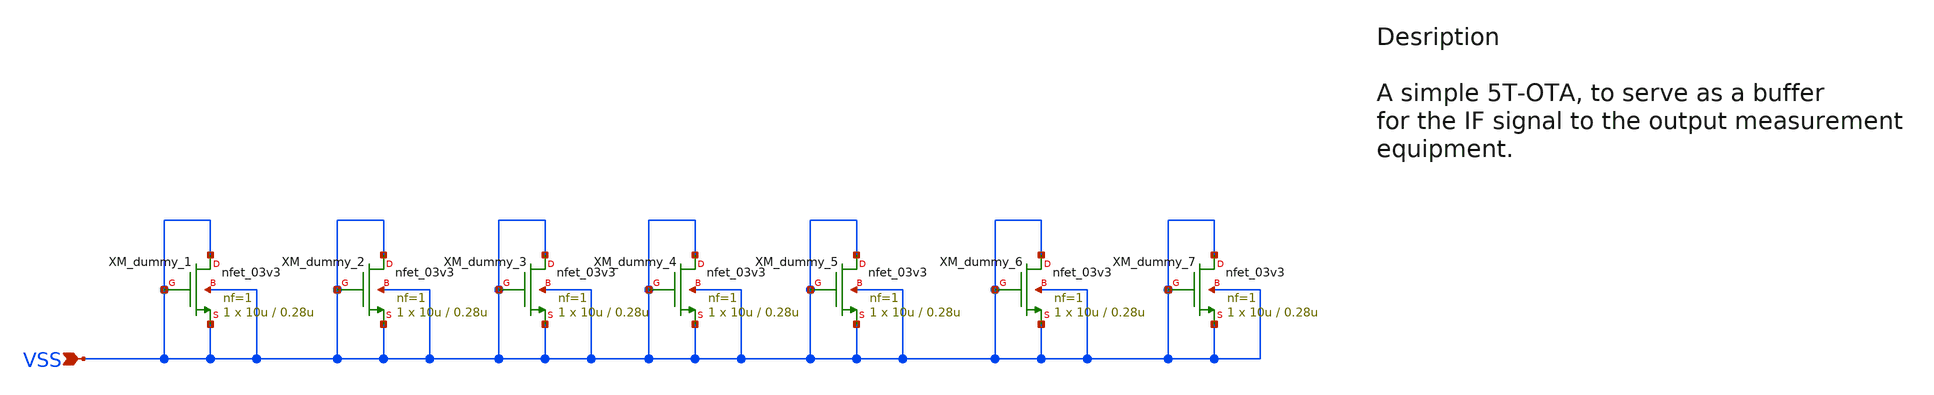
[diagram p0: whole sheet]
** sch_path: src/design_xsch/Dummy_devices_all.sch
**.subckt Dummy_devices_all VSS
*.ipin VSS
XM_dummy_1 VSS VSS VSS VSS nfet_03v3 L=0.28u W=10u nf=1 ad='int((nf+1)/2) * W/nf * 0.18u' as='int((nf+2)/2) * W/nf * 0.18u'
+ pd='2*int((nf+1)/2) * (W/nf + 0.18u)' ps='2*int((nf+2)/2) * (W/nf + 0.18u)' nrd='0.18u / W' nrs='0.18u / W'
+ sa=0 sb=0 sd=0 m=1
XM_dummy_2 VSS VSS VSS VSS nfet_03v3 L=0.28u W=10u nf=1 ad='int((nf+1)/2) * W/nf * 0.18u' as='int((nf+2)/2) * W/nf * 0.18u'
+ pd='2*int((nf+1)/2) * (W/nf + 0.18u)' ps='2*int((nf+2)/2) * (W/nf + 0.18u)' nrd='0.18u / W' nrs='0.18u / W'
+ sa=0 sb=0 sd=0 m=1
XM_dummy_3 VSS VSS VSS VSS nfet_03v3 L=0.28u W=10u nf=1 ad='int((nf+1)/2) * W/nf * 0.18u' as='int((nf+2)/2) * W/nf * 0.18u'
+ pd='2*int((nf+1)/2) * (W/nf + 0.18u)' ps='2*int((nf+2)/2) * (W/nf + 0.18u)' nrd='0.18u / W' nrs='0.18u / W'
+ sa=0 sb=0 sd=0 m=1
XM_dummy_4 VSS VSS VSS VSS nfet_03v3 L=0.28u W=10u nf=1 ad='int((nf+1)/2) * W/nf * 0.18u' as='int((nf+2)/2) * W/nf * 0.18u'
+ pd='2*int((nf+1)/2) * (W/nf + 0.18u)' ps='2*int((nf+2)/2) * (W/nf + 0.18u)' nrd='0.18u / W' nrs='0.18u / W'
+ sa=0 sb=0 sd=0 m=1
XM_dummy_5 VSS VSS VSS VSS nfet_03v3 L=0.28u W=10u nf=1 ad='int((nf+1)/2) * W/nf * 0.18u' as='int((nf+2)/2) * W/nf * 0.18u'
+ pd='2*int((nf+1)/2) * (W/nf + 0.18u)' ps='2*int((nf+2)/2) * (W/nf + 0.18u)' nrd='0.18u / W' nrs='0.18u / W'
+ sa=0 sb=0 sd=0 m=1
XM_dummy_6 VSS VSS VSS VSS nfet_03v3 L=0.28u W=10u nf=1 ad='int((nf+1)/2) * W/nf * 0.18u' as='int((nf+2)/2) * W/nf * 0.18u'
+ pd='2*int((nf+1)/2) * (W/nf + 0.18u)' ps='2*int((nf+2)/2) * (W/nf + 0.18u)' nrd='0.18u / W' nrs='0.18u / W'
+ sa=0 sb=0 sd=0 m=1
XM_dummy_7 VSS VSS VSS VSS nfet_03v3 L=0.28u W=10u nf=1 ad='int((nf+1)/2) * W/nf * 0.18u' as='int((nf+2)/2) * W/nf * 0.18u'
+ pd='2*int((nf+1)/2) * (W/nf + 0.18u)' ps='2*int((nf+2)/2) * (W/nf + 0.18u)' nrd='0.18u / W' nrs='0.18u / W'
+ sa=0 sb=0 sd=0 m=1
**** begin user architecture code

.include $::180MCU_MODELS/design.ngspice
.lib $::180MCU_MODELS/sm141064.ngspice typical
.lib $::180MCU_MODELS/sm141064.ngspice mimcap_typical
.lib $::180MCU_MODELS/sm141064.ngspice cap_mim
.lib $::180MCU_MODELS/sm141064.ngspice res_typical


**** end user architecture code
**.ends
.end
